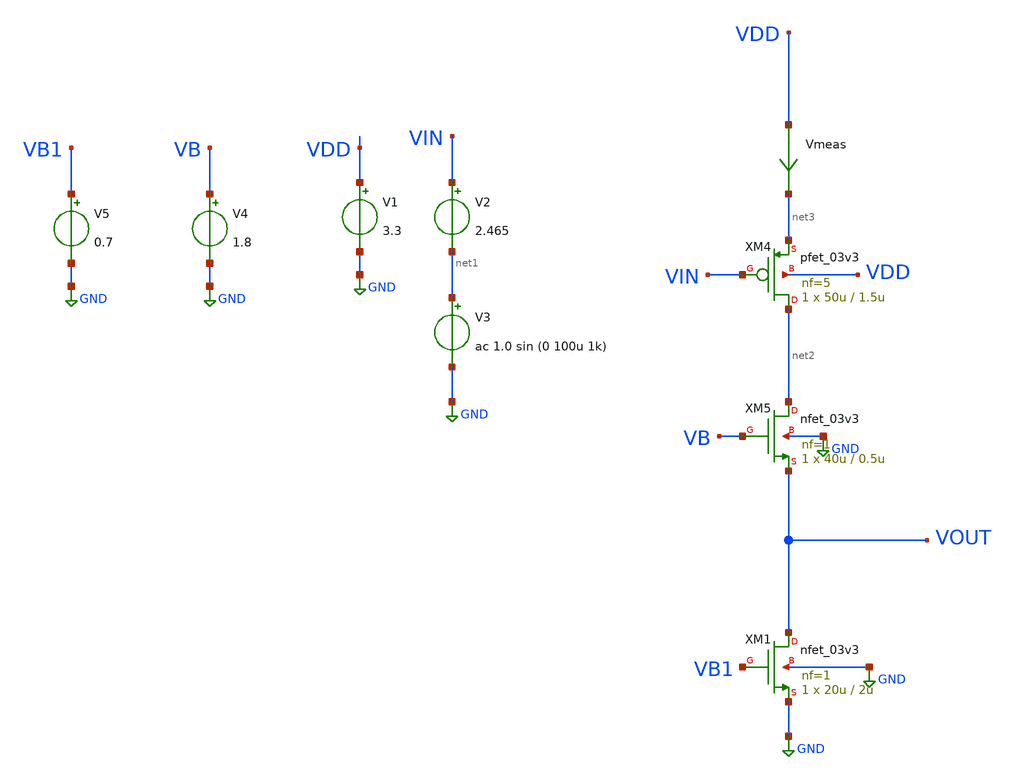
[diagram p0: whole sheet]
** sch_path: simple_amp14.sch
**.subckt simple_amp14
V1 VDD GND 3.3
V2 VIN net1 2.465
V3 net1 GND ac 1.0 sin (0 100u 1k)
V4 VB GND 1.8
V5 VB1 GND 0.7
XM4 net2 VIN net3 VDD pfet_03v3 L=1.5u W=50u nf=5 ad='int((nf+1)/2) * W/nf * 0.18u' as='int((nf+2)/2) * W/nf * 0.18u'
+ pd='2*int((nf+1)/2) * (W/nf + 0.18u)' ps='2*int((nf+2)/2) * (W/nf + 0.18u)' nrd='0.18u / W' nrs='0.18u / W'
+ sa=0 sb=0 sd=0 m=1
XM5 net2 VB VOUT GND nfet_03v3 L=0.5u W=40u nf=1 ad='int((nf+1)/2) * W/nf * 0.18u' as='int((nf+2)/2) * W/nf * 0.18u'
+ pd='2*int((nf+1)/2) * (W/nf + 0.18u)' ps='2*int((nf+2)/2) * (W/nf + 0.18u)' nrd='0.18u / W' nrs='0.18u / W'
+ sa=0 sb=0 sd=0 m=1
XM1 VOUT VB1 GND GND nfet_03v3 L=2u W=20u nf=1 ad='int((nf+1)/2) * W/nf * 0.18u' as='int((nf+2)/2) * W/nf * 0.18u'
+ pd='2*int((nf+1)/2) * (W/nf + 0.18u)' ps='2*int((nf+2)/2) * (W/nf + 0.18u)' nrd='0.18u / W' nrs='0.18u / W'
+ sa=0 sb=0 sd=0 m=1
Vmeas VDD net3 0
.save i(vmeas)
**** begin user architecture code

.include $::180MCU_MODELS/design.ngspice
*.lib $::180MCU_MODELS/sm141064.ngspice statistical
*.lib $::180MCU_MODELS/sm141064.ngspice res_statistical
.lib $::180MCU_MODELS/sm141064.ngspice typical
.lib $::180MCU_MODELS/sm141064.ngspice res_typical
.lib $::180MCU_MODELS/sm141064.ngspice moscap_typical
.lib $::180MCU_MODELS/sm141064.ngspice bjt_typical
.lib $::180MCU_MODELS/sm141064.ngspice diode_typical
.lib $::180MCU_MODELS/sm141064.ngspice mimcap_typical
.TEMP 27

.param   sw_stat_global = 1   sw_stat_mism = 1  mc_skew = 3  res_mc_skew = 3  cap_mc_skew = 3
+  fnoicor = 1



.control
save all
dc V2 0 3.3 0.01

plot v(Vc)
plot v(VOUT) deriv(v(VOUT)) v(VIN)
plot deriv(v(VOUT)) (v(VDD)-v(VG)) (v(VDD)-v(VOUT))
plot i(Vmeas)
plot deriv(v(VOUT))
tran 1u 5m
plot (v(VOUT)-0.55315) (v(VIN)-2.465)
plot fft((v(VOUT))) fft((v(VIN)))
ac dec 20 1 50G
plot v(VOUT)
.endc

**** end user architecture code
**.ends
.GLOBAL GND
.end
